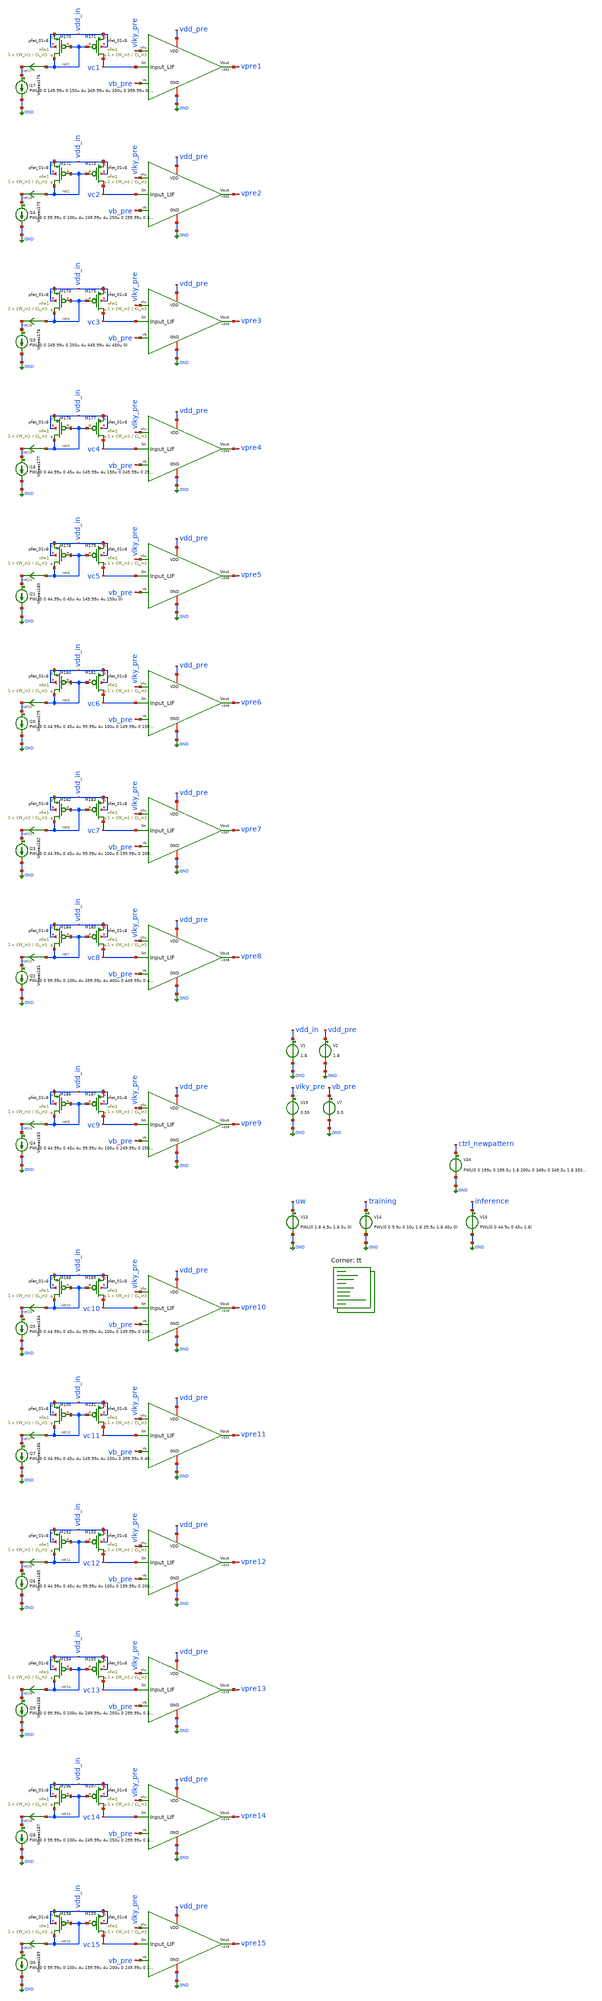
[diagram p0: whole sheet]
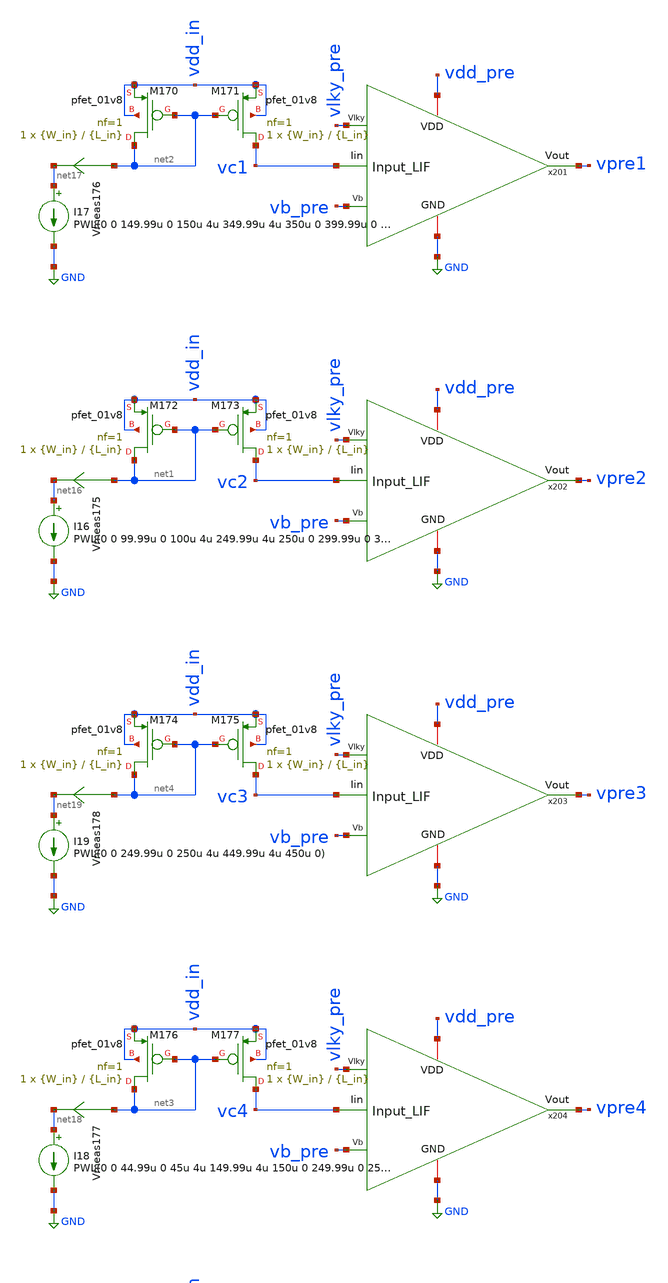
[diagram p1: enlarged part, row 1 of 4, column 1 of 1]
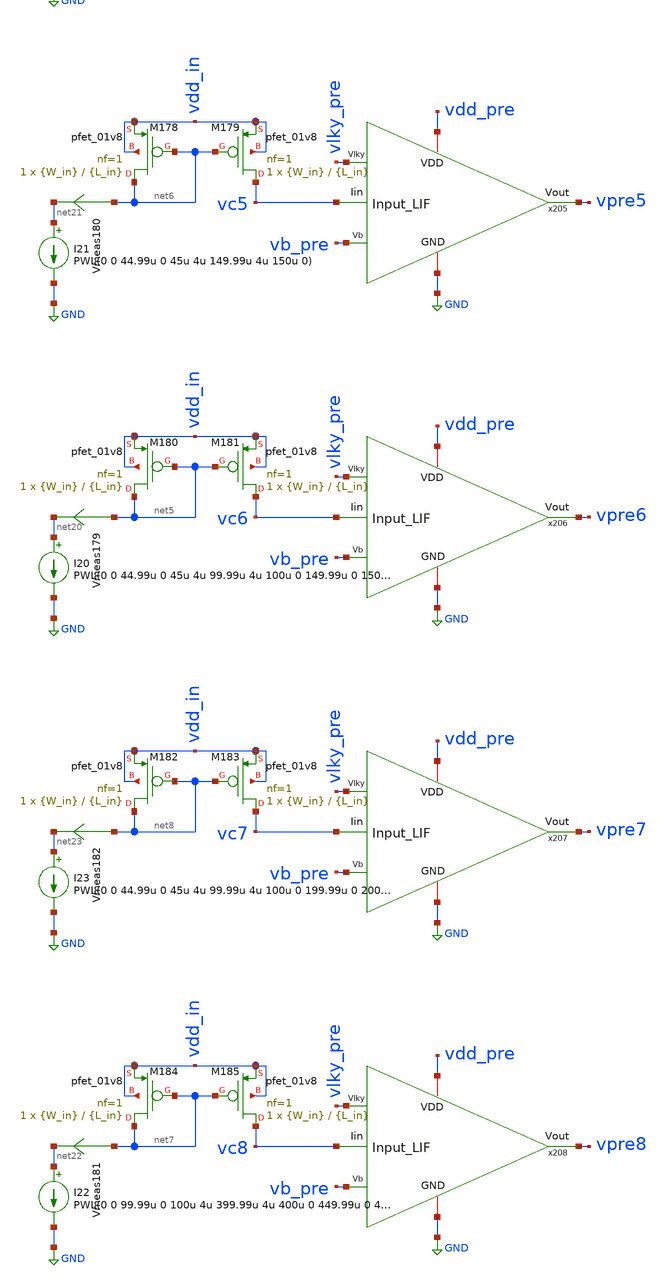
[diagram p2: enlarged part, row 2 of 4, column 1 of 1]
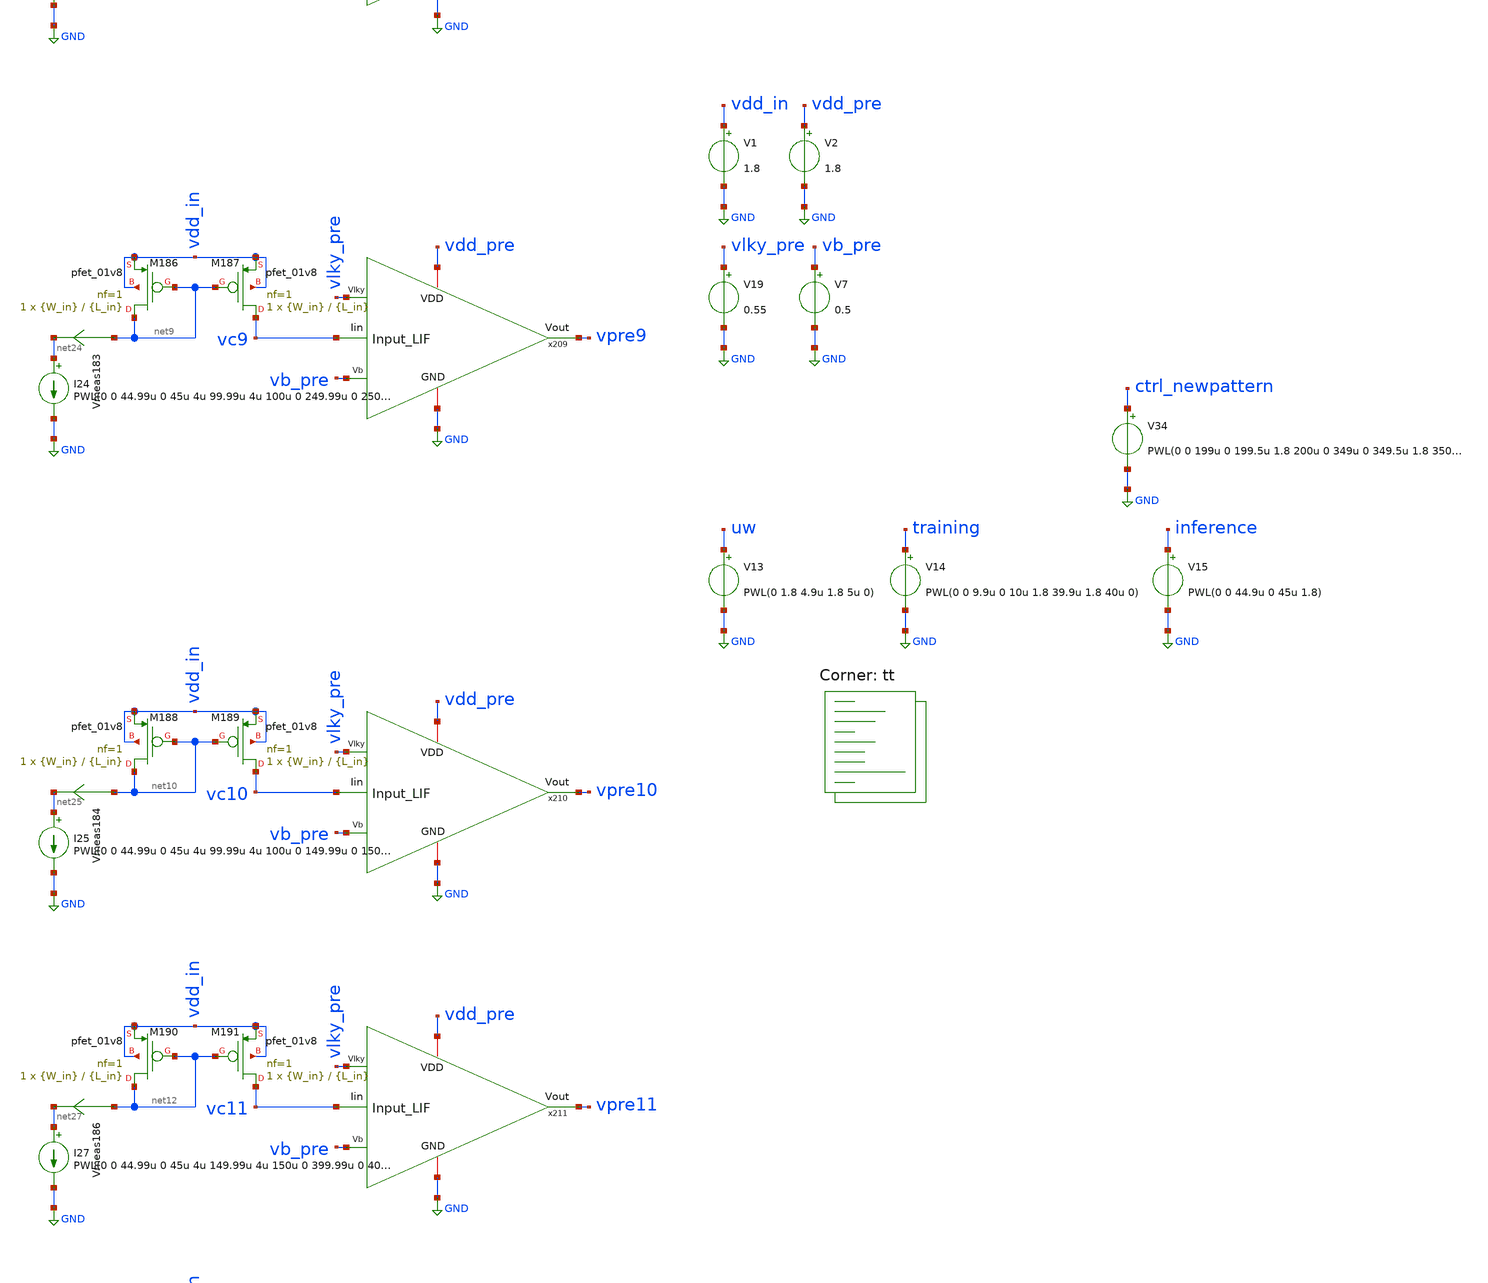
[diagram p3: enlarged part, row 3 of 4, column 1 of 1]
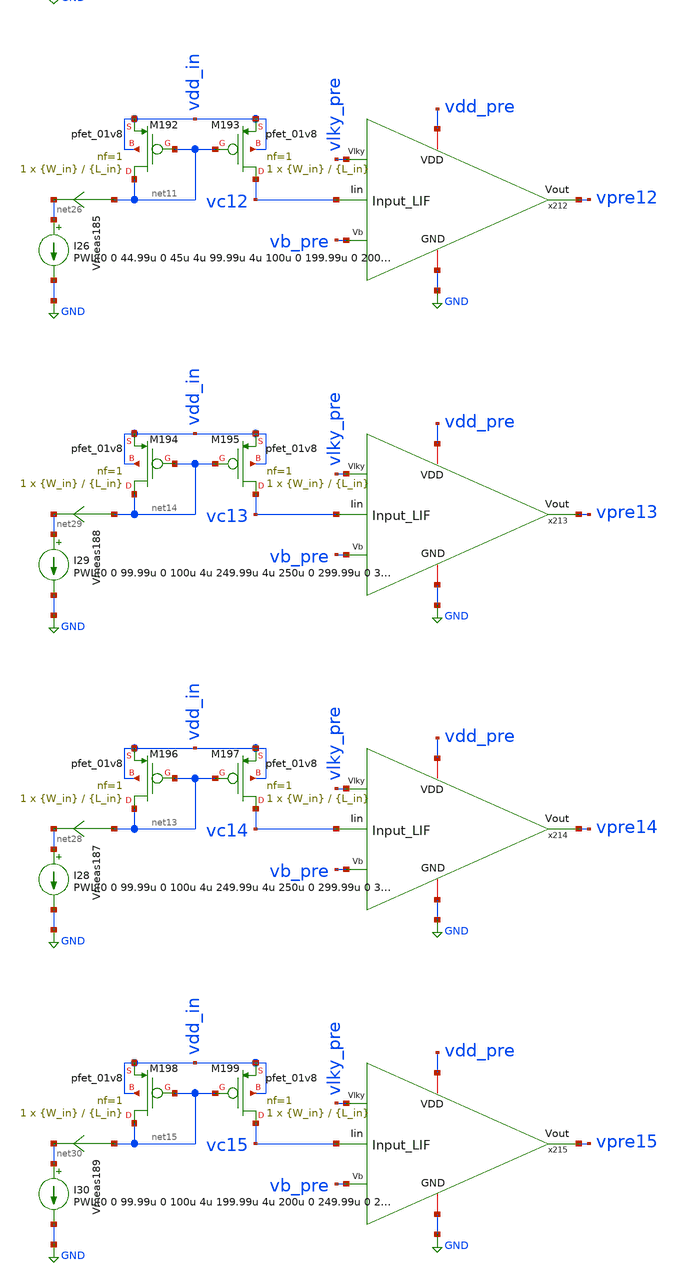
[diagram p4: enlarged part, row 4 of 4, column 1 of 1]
** sch_path: SNN/LIF_15Inputs_tb.sch
**.subckt LIF_15Inputs_tb
V1 vdd_in GND 1.8
V2 vdd_pre GND 1.8
XM173 vc2 net1 vdd_in vdd_in sky130_fd_pr__pfet_01v8 L={L_in} W={W_in} nf=1 ad='int((nf+1)/2) * W/nf * 0.29'
+ as='int((nf+2)/2) * W/nf * 0.29' pd='2*int((nf+1)/2) * (W/nf + 0.29)' ps='2*int((nf+2)/2) * (W/nf + 0.29)'
+ nrd='0.29 / W' nrs='0.29 / W' sa=0 sb=0 sd=0 mult=1 m=1
XM172 net1 net1 vdd_in vdd_in sky130_fd_pr__pfet_01v8 L={L_in} W={W_in} nf=1 ad='int((nf+1)/2) * W/nf * 0.29'
+ as='int((nf+2)/2) * W/nf * 0.29' pd='2*int((nf+1)/2) * (W/nf + 0.29)' ps='2*int((nf+2)/2) * (W/nf + 0.29)'
+ nrd='0.29 / W' nrs='0.29 / W' sa=0 sb=0 sd=0 mult=1 m=1
V13 uw GND PWL(0 1.8 4.9u 1.8 5u 0)
V14 training GND PWL(0 0 9.9u 0 10u 1.8 39.9u 1.8 40u 0)
V15 inference GND PWL(0 0 44.9u 0 45u 1.8)
V7 vb_pre GND 0.5
XM171 vc1 net2 vdd_in vdd_in sky130_fd_pr__pfet_01v8 L={L_in} W={W_in} nf=1 ad='int((nf+1)/2) * W/nf * 0.29'
+ as='int((nf+2)/2) * W/nf * 0.29' pd='2*int((nf+1)/2) * (W/nf + 0.29)' ps='2*int((nf+2)/2) * (W/nf + 0.29)'
+ nrd='0.29 / W' nrs='0.29 / W' sa=0 sb=0 sd=0 mult=1 m=1
XM170 net2 net2 vdd_in vdd_in sky130_fd_pr__pfet_01v8 L={L_in} W={W_in} nf=1 ad='int((nf+1)/2) * W/nf * 0.29'
+ as='int((nf+2)/2) * W/nf * 0.29' pd='2*int((nf+1)/2) * (W/nf + 0.29)' ps='2*int((nf+2)/2) * (W/nf + 0.29)'
+ nrd='0.29 / W' nrs='0.29 / W' sa=0 sb=0 sd=0 mult=1 m=1
V19 vlky_pre GND 0.55
XM177 vc4 net3 vdd_in vdd_in sky130_fd_pr__pfet_01v8 L={L_in} W={W_in} nf=1 ad='int((nf+1)/2) * W/nf * 0.29'
+ as='int((nf+2)/2) * W/nf * 0.29' pd='2*int((nf+1)/2) * (W/nf + 0.29)' ps='2*int((nf+2)/2) * (W/nf + 0.29)'
+ nrd='0.29 / W' nrs='0.29 / W' sa=0 sb=0 sd=0 mult=1 m=1
XM176 net3 net3 vdd_in vdd_in sky130_fd_pr__pfet_01v8 L={L_in} W={W_in} nf=1 ad='int((nf+1)/2) * W/nf * 0.29'
+ as='int((nf+2)/2) * W/nf * 0.29' pd='2*int((nf+1)/2) * (W/nf + 0.29)' ps='2*int((nf+2)/2) * (W/nf + 0.29)'
+ nrd='0.29 / W' nrs='0.29 / W' sa=0 sb=0 sd=0 mult=1 m=1
XM175 vc3 net4 vdd_in vdd_in sky130_fd_pr__pfet_01v8 L={L_in} W={W_in} nf=1 ad='int((nf+1)/2) * W/nf * 0.29'
+ as='int((nf+2)/2) * W/nf * 0.29' pd='2*int((nf+1)/2) * (W/nf + 0.29)' ps='2*int((nf+2)/2) * (W/nf + 0.29)'
+ nrd='0.29 / W' nrs='0.29 / W' sa=0 sb=0 sd=0 mult=1 m=1
XM174 net4 net4 vdd_in vdd_in sky130_fd_pr__pfet_01v8 L={L_in} W={W_in} nf=1 ad='int((nf+1)/2) * W/nf * 0.29'
+ as='int((nf+2)/2) * W/nf * 0.29' pd='2*int((nf+1)/2) * (W/nf + 0.29)' ps='2*int((nf+2)/2) * (W/nf + 0.29)'
+ nrd='0.29 / W' nrs='0.29 / W' sa=0 sb=0 sd=0 mult=1 m=1
XM181 vc6 net5 vdd_in vdd_in sky130_fd_pr__pfet_01v8 L={L_in} W={W_in} nf=1 ad='int((nf+1)/2) * W/nf * 0.29'
+ as='int((nf+2)/2) * W/nf * 0.29' pd='2*int((nf+1)/2) * (W/nf + 0.29)' ps='2*int((nf+2)/2) * (W/nf + 0.29)'
+ nrd='0.29 / W' nrs='0.29 / W' sa=0 sb=0 sd=0 mult=1 m=1
XM180 net5 net5 vdd_in vdd_in sky130_fd_pr__pfet_01v8 L={L_in} W={W_in} nf=1 ad='int((nf+1)/2) * W/nf * 0.29'
+ as='int((nf+2)/2) * W/nf * 0.29' pd='2*int((nf+1)/2) * (W/nf + 0.29)' ps='2*int((nf+2)/2) * (W/nf + 0.29)'
+ nrd='0.29 / W' nrs='0.29 / W' sa=0 sb=0 sd=0 mult=1 m=1
XM179 vc5 net6 vdd_in vdd_in sky130_fd_pr__pfet_01v8 L={L_in} W={W_in} nf=1 ad='int((nf+1)/2) * W/nf * 0.29'
+ as='int((nf+2)/2) * W/nf * 0.29' pd='2*int((nf+1)/2) * (W/nf + 0.29)' ps='2*int((nf+2)/2) * (W/nf + 0.29)'
+ nrd='0.29 / W' nrs='0.29 / W' sa=0 sb=0 sd=0 mult=1 m=1
XM178 net6 net6 vdd_in vdd_in sky130_fd_pr__pfet_01v8 L={L_in} W={W_in} nf=1 ad='int((nf+1)/2) * W/nf * 0.29'
+ as='int((nf+2)/2) * W/nf * 0.29' pd='2*int((nf+1)/2) * (W/nf + 0.29)' ps='2*int((nf+2)/2) * (W/nf + 0.29)'
+ nrd='0.29 / W' nrs='0.29 / W' sa=0 sb=0 sd=0 mult=1 m=1
XM185 vc8 net7 vdd_in vdd_in sky130_fd_pr__pfet_01v8 L={L_in} W={W_in} nf=1 ad='int((nf+1)/2) * W/nf * 0.29'
+ as='int((nf+2)/2) * W/nf * 0.29' pd='2*int((nf+1)/2) * (W/nf + 0.29)' ps='2*int((nf+2)/2) * (W/nf + 0.29)'
+ nrd='0.29 / W' nrs='0.29 / W' sa=0 sb=0 sd=0 mult=1 m=1
XM184 net7 net7 vdd_in vdd_in sky130_fd_pr__pfet_01v8 L={L_in} W={W_in} nf=1 ad='int((nf+1)/2) * W/nf * 0.29'
+ as='int((nf+2)/2) * W/nf * 0.29' pd='2*int((nf+1)/2) * (W/nf + 0.29)' ps='2*int((nf+2)/2) * (W/nf + 0.29)'
+ nrd='0.29 / W' nrs='0.29 / W' sa=0 sb=0 sd=0 mult=1 m=1
XM183 vc7 net8 vdd_in vdd_in sky130_fd_pr__pfet_01v8 L={L_in} W={W_in} nf=1 ad='int((nf+1)/2) * W/nf * 0.29'
+ as='int((nf+2)/2) * W/nf * 0.29' pd='2*int((nf+1)/2) * (W/nf + 0.29)' ps='2*int((nf+2)/2) * (W/nf + 0.29)'
+ nrd='0.29 / W' nrs='0.29 / W' sa=0 sb=0 sd=0 mult=1 m=1
XM182 net8 net8 vdd_in vdd_in sky130_fd_pr__pfet_01v8 L={L_in} W={W_in} nf=1 ad='int((nf+1)/2) * W/nf * 0.29'
+ as='int((nf+2)/2) * W/nf * 0.29' pd='2*int((nf+1)/2) * (W/nf + 0.29)' ps='2*int((nf+2)/2) * (W/nf + 0.29)'
+ nrd='0.29 / W' nrs='0.29 / W' sa=0 sb=0 sd=0 mult=1 m=1
XM187 vc9 net9 vdd_in vdd_in sky130_fd_pr__pfet_01v8 L={L_in} W={W_in} nf=1 ad='int((nf+1)/2) * W/nf * 0.29'
+ as='int((nf+2)/2) * W/nf * 0.29' pd='2*int((nf+1)/2) * (W/nf + 0.29)' ps='2*int((nf+2)/2) * (W/nf + 0.29)'
+ nrd='0.29 / W' nrs='0.29 / W' sa=0 sb=0 sd=0 mult=1 m=1
XM186 net9 net9 vdd_in vdd_in sky130_fd_pr__pfet_01v8 L={L_in} W={W_in} nf=1 ad='int((nf+1)/2) * W/nf * 0.29'
+ as='int((nf+2)/2) * W/nf * 0.29' pd='2*int((nf+1)/2) * (W/nf + 0.29)' ps='2*int((nf+2)/2) * (W/nf + 0.29)'
+ nrd='0.29 / W' nrs='0.29 / W' sa=0 sb=0 sd=0 mult=1 m=1
XM189 vc10 net10 vdd_in vdd_in sky130_fd_pr__pfet_01v8 L={L_in} W={W_in} nf=1 ad='int((nf+1)/2) * W/nf * 0.29'
+ as='int((nf+2)/2) * W/nf * 0.29' pd='2*int((nf+1)/2) * (W/nf + 0.29)' ps='2*int((nf+2)/2) * (W/nf + 0.29)'
+ nrd='0.29 / W' nrs='0.29 / W' sa=0 sb=0 sd=0 mult=1 m=1
XM188 net10 net10 vdd_in vdd_in sky130_fd_pr__pfet_01v8 L={L_in} W={W_in} nf=1 ad='int((nf+1)/2) * W/nf * 0.29'
+ as='int((nf+2)/2) * W/nf * 0.29' pd='2*int((nf+1)/2) * (W/nf + 0.29)' ps='2*int((nf+2)/2) * (W/nf + 0.29)'
+ nrd='0.29 / W' nrs='0.29 / W' sa=0 sb=0 sd=0 mult=1 m=1
XM193 vc12 net11 vdd_in vdd_in sky130_fd_pr__pfet_01v8 L={L_in} W={W_in} nf=1 ad='int((nf+1)/2) * W/nf * 0.29'
+ as='int((nf+2)/2) * W/nf * 0.29' pd='2*int((nf+1)/2) * (W/nf + 0.29)' ps='2*int((nf+2)/2) * (W/nf + 0.29)'
+ nrd='0.29 / W' nrs='0.29 / W' sa=0 sb=0 sd=0 mult=1 m=1
XM192 net11 net11 vdd_in vdd_in sky130_fd_pr__pfet_01v8 L={L_in} W={W_in} nf=1 ad='int((nf+1)/2) * W/nf * 0.29'
+ as='int((nf+2)/2) * W/nf * 0.29' pd='2*int((nf+1)/2) * (W/nf + 0.29)' ps='2*int((nf+2)/2) * (W/nf + 0.29)'
+ nrd='0.29 / W' nrs='0.29 / W' sa=0 sb=0 sd=0 mult=1 m=1
XM191 vc11 net12 vdd_in vdd_in sky130_fd_pr__pfet_01v8 L={L_in} W={W_in} nf=1 ad='int((nf+1)/2) * W/nf * 0.29'
+ as='int((nf+2)/2) * W/nf * 0.29' pd='2*int((nf+1)/2) * (W/nf + 0.29)' ps='2*int((nf+2)/2) * (W/nf + 0.29)'
+ nrd='0.29 / W' nrs='0.29 / W' sa=0 sb=0 sd=0 mult=1 m=1
XM190 net12 net12 vdd_in vdd_in sky130_fd_pr__pfet_01v8 L={L_in} W={W_in} nf=1 ad='int((nf+1)/2) * W/nf * 0.29'
+ as='int((nf+2)/2) * W/nf * 0.29' pd='2*int((nf+1)/2) * (W/nf + 0.29)' ps='2*int((nf+2)/2) * (W/nf + 0.29)'
+ nrd='0.29 / W' nrs='0.29 / W' sa=0 sb=0 sd=0 mult=1 m=1
XM197 vc14 net13 vdd_in vdd_in sky130_fd_pr__pfet_01v8 L={L_in} W={W_in} nf=1 ad='int((nf+1)/2) * W/nf * 0.29'
+ as='int((nf+2)/2) * W/nf * 0.29' pd='2*int((nf+1)/2) * (W/nf + 0.29)' ps='2*int((nf+2)/2) * (W/nf + 0.29)'
+ nrd='0.29 / W' nrs='0.29 / W' sa=0 sb=0 sd=0 mult=1 m=1
XM196 net13 net13 vdd_in vdd_in sky130_fd_pr__pfet_01v8 L={L_in} W={W_in} nf=1 ad='int((nf+1)/2) * W/nf * 0.29'
+ as='int((nf+2)/2) * W/nf * 0.29' pd='2*int((nf+1)/2) * (W/nf + 0.29)' ps='2*int((nf+2)/2) * (W/nf + 0.29)'
+ nrd='0.29 / W' nrs='0.29 / W' sa=0 sb=0 sd=0 mult=1 m=1
XM195 vc13 net14 vdd_in vdd_in sky130_fd_pr__pfet_01v8 L={L_in} W={W_in} nf=1 ad='int((nf+1)/2) * W/nf * 0.29'
+ as='int((nf+2)/2) * W/nf * 0.29' pd='2*int((nf+1)/2) * (W/nf + 0.29)' ps='2*int((nf+2)/2) * (W/nf + 0.29)'
+ nrd='0.29 / W' nrs='0.29 / W' sa=0 sb=0 sd=0 mult=1 m=1
XM194 net14 net14 vdd_in vdd_in sky130_fd_pr__pfet_01v8 L={L_in} W={W_in} nf=1 ad='int((nf+1)/2) * W/nf * 0.29'
+ as='int((nf+2)/2) * W/nf * 0.29' pd='2*int((nf+1)/2) * (W/nf + 0.29)' ps='2*int((nf+2)/2) * (W/nf + 0.29)'
+ nrd='0.29 / W' nrs='0.29 / W' sa=0 sb=0 sd=0 mult=1 m=1
XM199 vc15 net15 vdd_in vdd_in sky130_fd_pr__pfet_01v8 L={L_in} W={W_in} nf=1 ad='int((nf+1)/2) * W/nf * 0.29'
+ as='int((nf+2)/2) * W/nf * 0.29' pd='2*int((nf+1)/2) * (W/nf + 0.29)' ps='2*int((nf+2)/2) * (W/nf + 0.29)'
+ nrd='0.29 / W' nrs='0.29 / W' sa=0 sb=0 sd=0 mult=1 m=1
XM198 net15 net15 vdd_in vdd_in sky130_fd_pr__pfet_01v8 L={L_in} W={W_in} nf=1 ad='int((nf+1)/2) * W/nf * 0.29'
+ as='int((nf+2)/2) * W/nf * 0.29' pd='2*int((nf+1)/2) * (W/nf + 0.29)' ps='2*int((nf+2)/2) * (W/nf + 0.29)'
+ nrd='0.29 / W' nrs='0.29 / W' sa=0 sb=0 sd=0 mult=1 m=1
V34 ctrl_newpattern GND PWL(0 0 199u 0 199.5u 1.8 200u 0 349u 0 349.5u 1.8 350u 0 499u 0 499.5u 1.8
+ 500u 0 649u 0 649.5u 1.8 650u 0 799u 0 799.5u 1.8 800u 0 949u 0 949.5u 1.8 950u 0 1099u 0 1099.5u 1.8
+ 1100u 0 1249u 0 1249.5u 1.8 1250u 0 1399u 0 1399.5u 1.8 1400u 0)
x201 vlky_pre vb_pre vdd_pre vpre1 GND vc1 Input_LIF
x202 vlky_pre vb_pre vdd_pre vpre2 GND vc2 Input_LIF
x203 vlky_pre vb_pre vdd_pre vpre3 GND vc3 Input_LIF
x204 vlky_pre vb_pre vdd_pre vpre4 GND vc4 Input_LIF
x205 vlky_pre vb_pre vdd_pre vpre5 GND vc5 Input_LIF
x206 vlky_pre vb_pre vdd_pre vpre6 GND vc6 Input_LIF
x207 vlky_pre vb_pre vdd_pre vpre7 GND vc7 Input_LIF
x208 vlky_pre vb_pre vdd_pre vpre8 GND vc8 Input_LIF
x209 vlky_pre vb_pre vdd_pre vpre9 GND vc9 Input_LIF
x210 vlky_pre vb_pre vdd_pre vpre10 GND vc10 Input_LIF
x211 vlky_pre vb_pre vdd_pre vpre11 GND vc11 Input_LIF
x212 vlky_pre vb_pre vdd_pre vpre12 GND vc12 Input_LIF
x213 vlky_pre vb_pre vdd_pre vpre13 GND vc13 Input_LIF
x214 vlky_pre vb_pre vdd_pre vpre14 GND vc14 Input_LIF
x215 vlky_pre vb_pre vdd_pre vpre15 GND vc15 Input_LIF
I16 net16 GND PWL(0 0 99.99u 0 100u 4u 249.99u 4u 250u 0 299.99u 0 300u 4u)
Vmeas175 net1 net16 0
.save i(vmeas175)
I17 net17 GND PWL(0 0 149.99u 0 150u 4u 349.99u 4u 350u 0 399.99u 0 400u 4u 449.99u 4u 450u 0)
Vmeas176 net2 net17 0
.save i(vmeas176)
I18 net18 GND PWL(0 0 44.99u 0 45u 4u 149.99u 4u 150u 0 249.99u 0 250u 4u 399.99u 4u 400u 0 449.99u
+ 0 450u 4u)
Vmeas177 net3 net18 0
.save i(vmeas177)
I19 net19 GND PWL(0 0 249.99u 0 250u 4u 449.99u 4u 450u 0)
Vmeas178 net4 net19 0
.save i(vmeas178)
I20 net20 GND PWL(0 0 44.99u 0 45u 4u 99.99u 4u 100u 0 149.99u 0 150u 4u 299.99u 4u 300u 0 399.99u 0
+ 400u 4u)
Vmeas179 net5 net20 0
.save i(vmeas179)
I21 net21 GND PWL(0 0 44.99u 0 45u 4u 149.99u 4u 150u 0)
Vmeas180 net6 net21 0
.save i(vmeas180)
I22 net22 GND PWL(0 0 99.99u 0 100u 4u 399.99u 4u 400u 0 449.99u 0 450u 4u)
Vmeas181 net7 net22 0
.save i(vmeas181)
I23 net23 GND PWL(0 0 44.99u 0 45u 4u 99.99u 4u 100u 0 199.99u 0 200u 4u 249.99u 4u 250u 0 349.99u 0
+ 350u 4u 399.99u 4u 400u 0)
Vmeas182 net8 net23 0
.save i(vmeas182)
I24 net24 GND PWL(0 0 44.99u 0 45u 4u 99.99u 4u 100u 0 249.99u 0 250u 4u 299.99u 4u 300u 0 399.99u 0
+ 400u 4u 449.99u 4u 450u 0 499.99u 0 500u 4u)
Vmeas183 net9 net24 0
.save i(vmeas183)
I25 net25 GND PWL(0 0 44.99u 0 45u 4u 99.99u 4u 100u 0 149.99u 0 150u 4u 199.99u 4u 200u 0 349.99u 0
+ 350u 4u 399.99u 4u 400u 0 449.99u 0 450u 4u 499.99u 4u 500u 0)
Vmeas184 net10 net25 0
.save i(vmeas184)
I26 net26 GND PWL(0 0 44.99u 0 45u 4u 99.99u 4u 100u 0 199.99u 0 200u 4u 399.99u 4u 400u 0 449.99u 0
+ 450u 4u)
Vmeas185 net11 net26 0
.save i(vmeas185)
I27 net27 GND PWL(0 0 44.99u 0 45u 4u 149.99u 4u 150u 0 399.99u 0 400u 4u 449.99u 4u 450u 0)
Vmeas186 net12 net27 0
.save i(vmeas186)
I28 net28 GND PWL(0 0 99.99u 0 100u 4u 249.99u 4u 250u 0 299.99u 0 300u 4u 399.99u 4u 400u 0 449.99u
+ 0 450u 4u 499.99u 4u 500u 0)
Vmeas187 net13 net28 0
.save i(vmeas187)
I29 net29 GND PWL(0 0 99.99u 0 100u 4u 249.99u 4u 250u 0 299.99u 0 300u 4u 349.99u 4u 350u 0 399.99u
+ 0 400u 4u 449.99u 4u 450u 0)
Vmeas188 net14 net29 0
.save i(vmeas188)
I30 net30 GND PWL(0 0 99.99u 0 100u 4u 199.99u 4u 200u 0 249.99u 0 250u 4u 299.99u 4u 300u 0 499.99u
+ 0 500u 4u)
Vmeas189 net15 net30 0
.save i(vmeas189)
**** begin user architecture code
.lib $::SKYWATER_MODELS/sky130.lib.spice tt

** opencircuitdesign pdks install
.inc $::SKYWATER_MODELS/rram_v0.spice



.option set_threads = 16
.option klu
*--Current Injection--*
.param L_in=0.15
.param W_in=1
.control
	save all
	tran 100n 1550u 0
	write LIF_15Inputs_tb.raw v(vpre1) v(vpre2) v(vpre3) v(vpre4) v(vpre5) v(vpre6) v(vpre7) v(vpre8)
+ v(vpre9) v(vpre10) v(vpre11) v(vpre12) v(vpre13) v(vpre14) v(vpre15) v(ctrl_newpattern)
	*wrdata SNN_15x1_lt_tb.ssv v(8)
.endc


**** end user architecture code
**.ends

* expanding   symbol:  /home/ricardo/RATT_repos/Proyectos_xschem/SNN/Input_LIF.sym # of pins=6
** sym_path: Final_Design/Input_LIF.sym
** sch_path: Final_Design/Input_LIF.sch
.subckt Input_LIF Vlky Vb VDD Vout GND Iin
*.iopin GND
*.ipin Vb
*.iopin VDD
*.opin Vout
*.ipin Iin
*.ipin Vlky
XM5 net3 Vb GND GND sky130_fd_pr__nfet_01v8 L=0.15 W=5 nf=1 ad='int((nf+1)/2) * W/nf * 0.29' as='int((nf+2)/2) * W/nf * 0.29'
+ pd='2*int((nf+1)/2) * (W/nf + 0.29)' ps='2*int((nf+2)/2) * (W/nf + 0.29)' nrd='0.29 / W' nrs='0.29 / W'
+ sa=0 sb=0 sd=0 mult=1 m=1
XM4 net1 net2 net3 GND sky130_fd_pr__nfet_01v8 L=0.15 W=1.5 nf=1 ad='int((nf+1)/2) * W/nf * 0.29' as='int((nf+2)/2) * W/nf * 0.29'
+ pd='2*int((nf+1)/2) * (W/nf + 0.29)' ps='2*int((nf+2)/2) * (W/nf + 0.29)' nrd='0.29 / W' nrs='0.29 / W'
+ sa=0 sb=0 sd=0 mult=1 m=1
XM3 net1 net2 VDD VDD sky130_fd_pr__pfet_01v8 L=20 W=1 nf=1 ad='int((nf+1)/2) * W/nf * 0.29' as='int((nf+2)/2) * W/nf * 0.29'
+ pd='2*int((nf+1)/2) * (W/nf + 0.29)' ps='2*int((nf+2)/2) * (W/nf + 0.29)' nrd='0.29 / W' nrs='0.29 / W'
+ sa=0 sb=0 sd=0 mult=1 m=1
XC2 net1 GND sky130_fd_pr__cap_mim_m3_1 W=10 L=5 MF=1 m=1
XM2 Iin net1 GND GND sky130_fd_pr__nfet_01v8 L=20 W=1 nf=1 ad='int((nf+1)/2) * W/nf * 0.29' as='int((nf+2)/2) * W/nf * 0.29'
+ pd='2*int((nf+1)/2) * (W/nf + 0.29)' ps='2*int((nf+2)/2) * (W/nf + 0.29)' nrd='0.29 / W' nrs='0.29 / W'
+ sa=0 sb=0 sd=0 mult=1 m=1
XC1 Iin GND sky130_fd_pr__cap_mim_m3_1 W=20 L=20 MF=1 m=1
XM10 net4 Vout GND GND sky130_fd_pr__nfet_01v8 L=0.15 W=1.5 nf=1 ad='int((nf+1)/2) * W/nf * 0.29' as='int((nf+2)/2) * W/nf * 0.29'
+ pd='2*int((nf+1)/2) * (W/nf + 0.29)' ps='2*int((nf+2)/2) * (W/nf + 0.29)' nrd='0.29 / W' nrs='0.29 / W'
+ sa=0 sb=0 sd=0 mult=1 m=1
XM7 net2 Iin net4 GND sky130_fd_pr__nfet_01v8 L=0.15 W=1.5 nf=1 ad='int((nf+1)/2) * W/nf * 0.29' as='int((nf+2)/2) * W/nf * 0.29'
+ pd='2*int((nf+1)/2) * (W/nf + 0.29)' ps='2*int((nf+2)/2) * (W/nf + 0.29)' nrd='0.29 / W' nrs='0.29 / W'
+ sa=0 sb=0 sd=0 mult=1 m=1
XM6 net2 Iin VDD VDD sky130_fd_pr__pfet_01v8 L=0.15 W=1.5 nf=1 ad='int((nf+1)/2) * W/nf * 0.29' as='int((nf+2)/2) * W/nf * 0.29'
+ pd='2*int((nf+1)/2) * (W/nf + 0.29)' ps='2*int((nf+2)/2) * (W/nf + 0.29)' nrd='0.29 / W' nrs='0.29 / W'
+ sa=0 sb=0 sd=0 mult=1 m=1
XM9 Vout net2 net4 GND sky130_fd_pr__nfet_01v8 L=0.15 W=1.5 nf=1 ad='int((nf+1)/2) * W/nf * 0.29' as='int((nf+2)/2) * W/nf * 0.29'
+ pd='2*int((nf+1)/2) * (W/nf + 0.29)' ps='2*int((nf+2)/2) * (W/nf + 0.29)' nrd='0.29 / W' nrs='0.29 / W'
+ sa=0 sb=0 sd=0 mult=1 m=1
XM8 Vout net2 VDD VDD sky130_fd_pr__pfet_01v8 L=0.15 W=5 nf=1 ad='int((nf+1)/2) * W/nf * 0.29' as='int((nf+2)/2) * W/nf * 0.29'
+ pd='2*int((nf+1)/2) * (W/nf + 0.29)' ps='2*int((nf+2)/2) * (W/nf + 0.29)' nrd='0.29 / W' nrs='0.29 / W'
+ sa=0 sb=0 sd=0 mult=1 m=1
XM1 Iin Vlky GND GND sky130_fd_pr__nfet_01v8 L=0.15 W=1.5 nf=1 ad='int((nf+1)/2) * W/nf * 0.29' as='int((nf+2)/2) * W/nf * 0.29'
+ pd='2*int((nf+1)/2) * (W/nf + 0.29)' ps='2*int((nf+2)/2) * (W/nf + 0.29)' nrd='0.29 / W' nrs='0.29 / W'
+ sa=0 sb=0 sd=0 mult=1 m=1
.ends

.GLOBAL GND
.end
